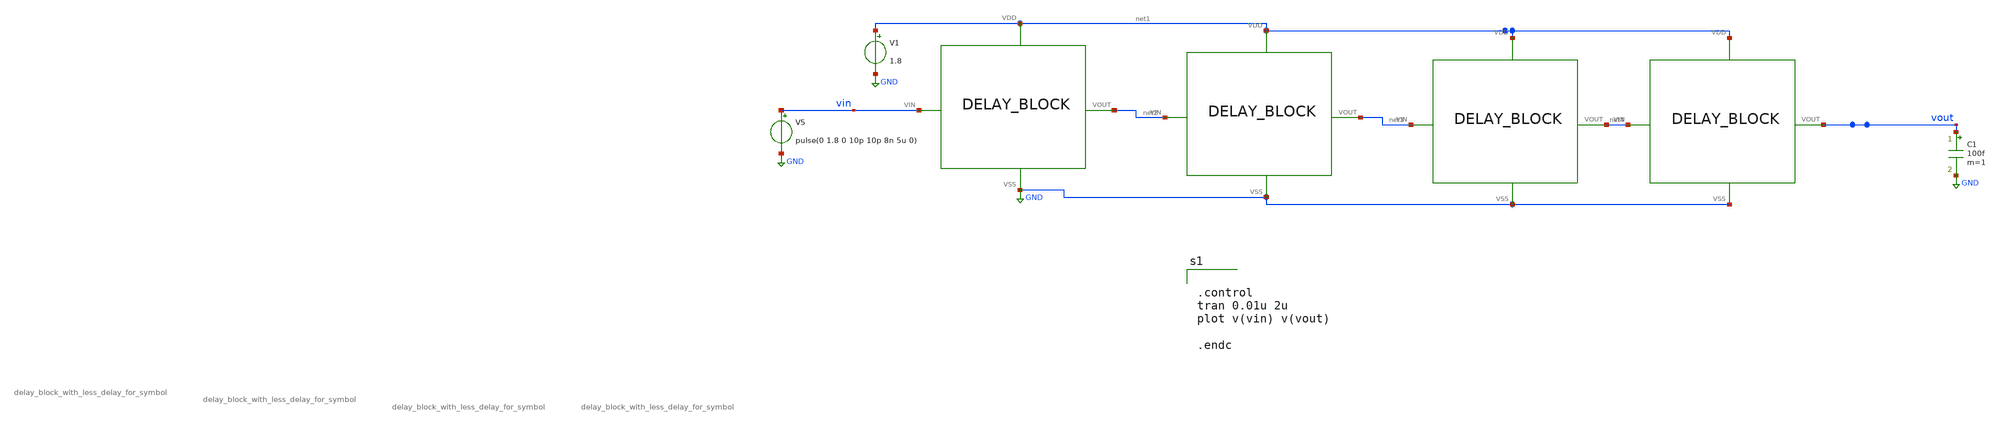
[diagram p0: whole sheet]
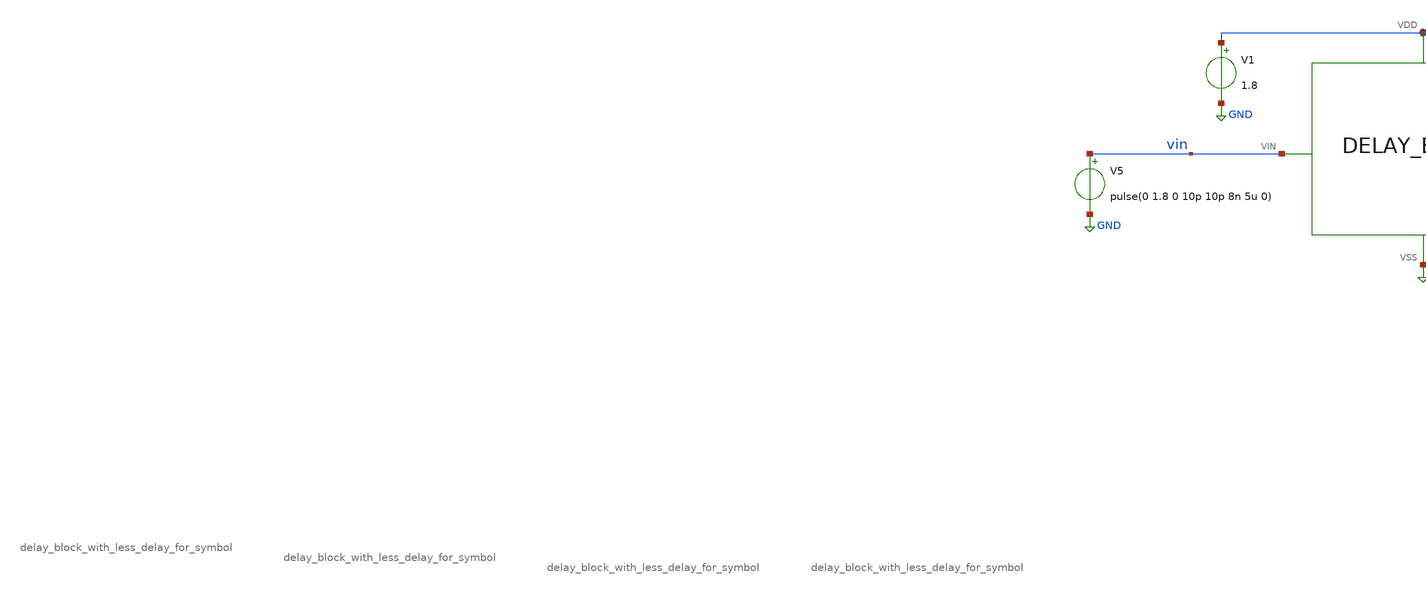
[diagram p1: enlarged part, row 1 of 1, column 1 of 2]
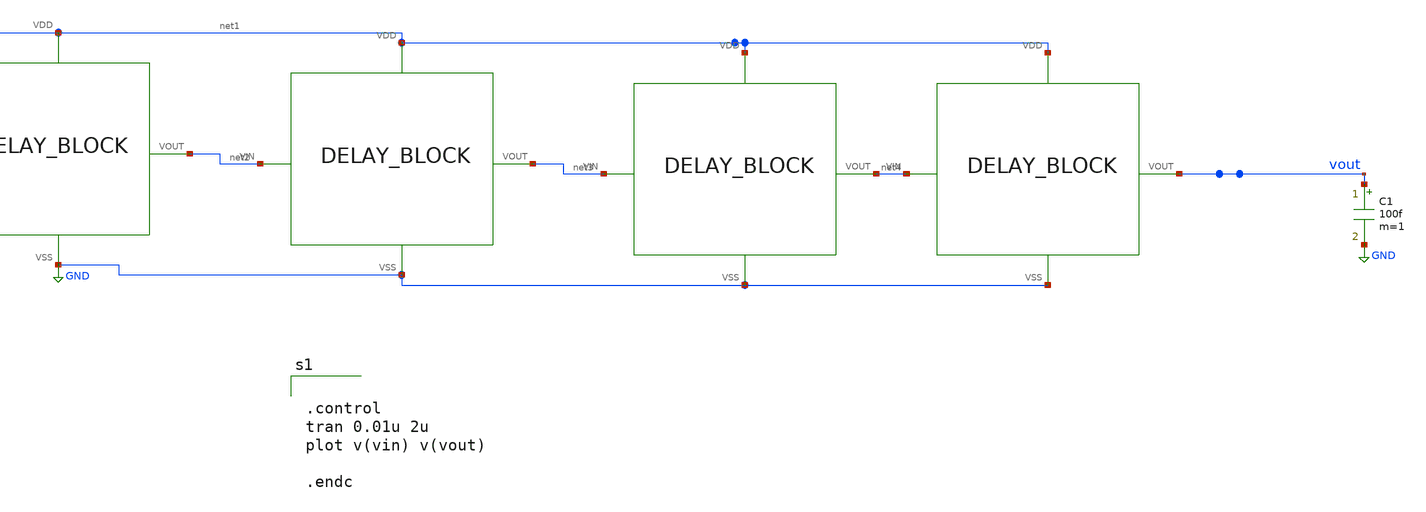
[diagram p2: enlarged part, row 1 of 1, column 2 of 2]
** sch_path: xschem/DC_DC_Converter_xschem/OTHERS/DC_DC_Converter_6/revised_delay-block/delay_bpock_tb.sch
**.subckt delay_bpock_tb
V1 net1 GND 1.8
V5 vin GND pulse(0 1.8 0 10p 10p 8n 5u 0)
C1 vout GND 100f m=1
X1 vin net2 net1 GND delay_block_with_less_delay_for_symbol
X2 net2 net3 net1 GND delay_block_with_less_delay_for_symbol
X3 net3 net4 net1 GND delay_block_with_less_delay_for_symbol
X4 net4 vout net1 GND delay_block_with_less_delay_for_symbol
**** begin user architecture code


.control
tran 0.01u 2u
plot v(vin) v(vout)

.endc



** opencircuitdesign pdks install
.lib $::SKYWATER_MODELS/sky130.lib.spice tt


**** end user architecture code
**.ends
.GLOBAL GND
.end
